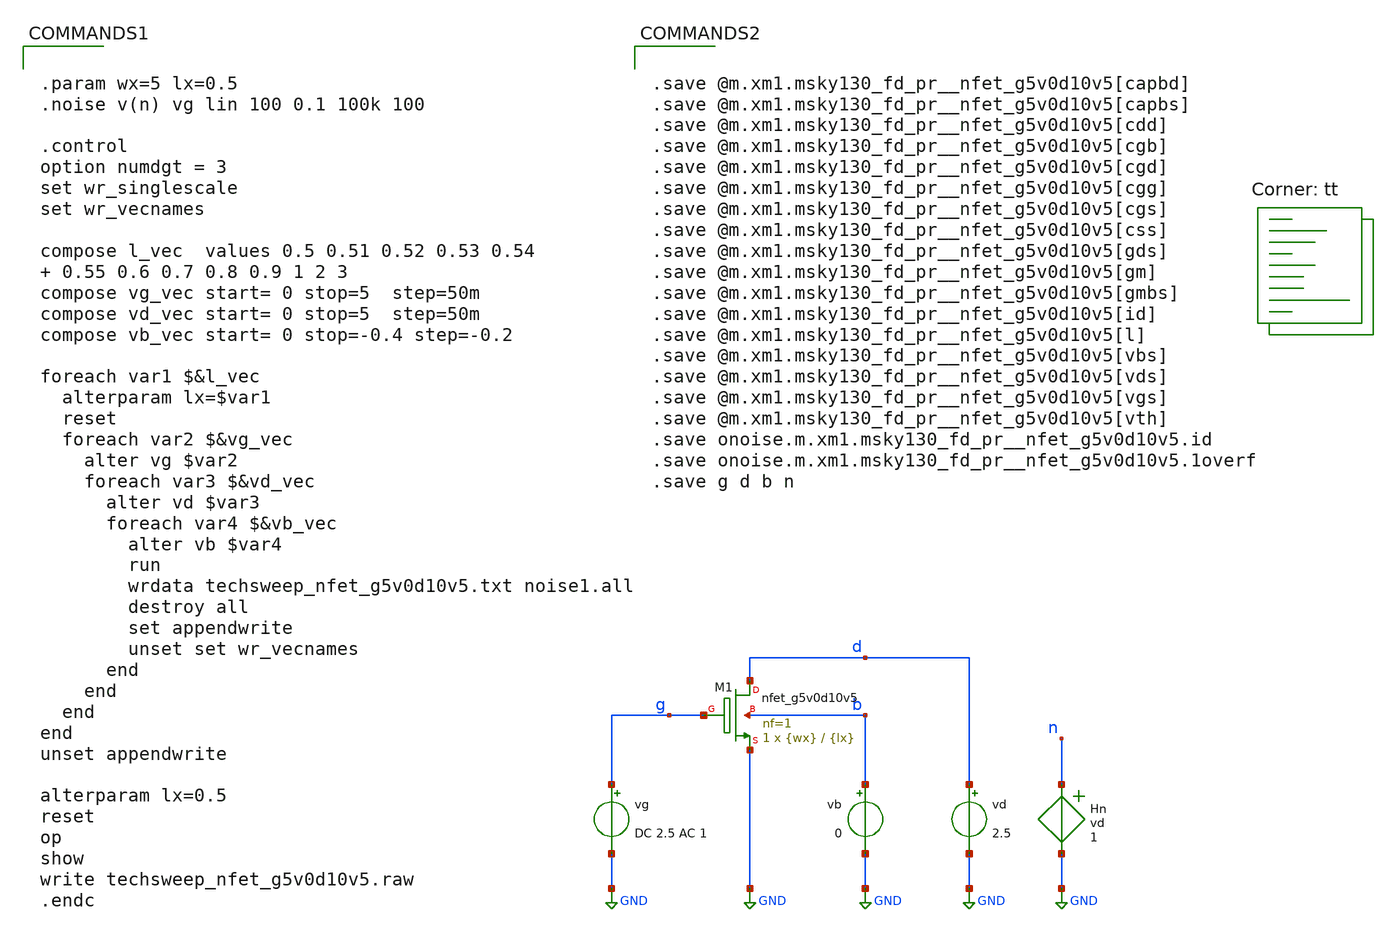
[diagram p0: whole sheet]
** sch_path: xschem/techsweep_nfet_g5v0d10v5.sch
**.subckt techsweep_nfet_g5v0d10v5
vg g GND DC 2.5 AC 1
vd d GND 2.5
vb b GND 0
Hn n GND vd 1
XM1 d g GND b sky130_fd_pr__nfet_g5v0d10v5 L={lx} W={wx} nf=1 ad='int((nf+1)/2) * W/nf * 0.29' as='int((nf+2)/2) * W/nf * 0.29'
+ pd='2*int((nf+1)/2) * (W/nf + 0.29)' ps='2*int((nf+2)/2) * (W/nf + 0.29)' nrd='0.29 / W' nrs='0.29 / W'
+ sa=0 sb=0 sd=0 mult=1 m=1
**** begin user architecture code


.param wx=5 lx=0.5
.noise v(n) vg lin 100 0.1 100k 100

.control
option numdgt = 3
set wr_singlescale
set wr_vecnames

compose l_vec  values 0.5 0.51 0.52 0.53 0.54  0.55 0.6 0.7 0.8 0.9 1 2 3
compose vg_vec start= 0 stop=5  step=50m
compose vd_vec start= 0 stop=5  step=50m
compose vb_vec start= 0 stop=-0.4 step=-0.2

foreach var1 $&l_vec
  alterparam lx=$var1
  reset
  foreach var2 $&vg_vec
    alter vg $var2
    foreach var3 $&vd_vec
      alter vd $var3
      foreach var4 $&vb_vec
        alter vb $var4
        run
        wrdata techsweep_nfet_g5v0d10v5.txt noise1.all
        destroy all
        set appendwrite
        unset set wr_vecnames
      end
    end
  end
end
unset appendwrite

alterparam lx=0.5
reset
op
show
write techsweep_nfet_g5v0d10v5.raw
.endc


.lib $::SKYWATER_MODELS/sky130.lib.spice tt


.save @m.xm1.msky130_fd_pr__nfet_g5v0d10v5[capbd]
.save @m.xm1.msky130_fd_pr__nfet_g5v0d10v5[capbs]
.save @m.xm1.msky130_fd_pr__nfet_g5v0d10v5[cdd]
.save @m.xm1.msky130_fd_pr__nfet_g5v0d10v5[cgb]
.save @m.xm1.msky130_fd_pr__nfet_g5v0d10v5[cgd]
.save @m.xm1.msky130_fd_pr__nfet_g5v0d10v5[cgg]
.save @m.xm1.msky130_fd_pr__nfet_g5v0d10v5[cgs]
.save @m.xm1.msky130_fd_pr__nfet_g5v0d10v5[css]
.save @m.xm1.msky130_fd_pr__nfet_g5v0d10v5[gds]
.save @m.xm1.msky130_fd_pr__nfet_g5v0d10v5[gm]
.save @m.xm1.msky130_fd_pr__nfet_g5v0d10v5[gmbs]
.save @m.xm1.msky130_fd_pr__nfet_g5v0d10v5[id]
.save @m.xm1.msky130_fd_pr__nfet_g5v0d10v5[l]
.save @m.xm1.msky130_fd_pr__nfet_g5v0d10v5[vbs]
.save @m.xm1.msky130_fd_pr__nfet_g5v0d10v5[vds]
.save @m.xm1.msky130_fd_pr__nfet_g5v0d10v5[vgs]
.save @m.xm1.msky130_fd_pr__nfet_g5v0d10v5[vth]
.save onoise.m.xm1.msky130_fd_pr__nfet_g5v0d10v5.id
.save onoise.m.xm1.msky130_fd_pr__nfet_g5v0d10v5.1overf
.save g d b n


**** end user architecture code
**.ends
.GLOBAL GND
.end
